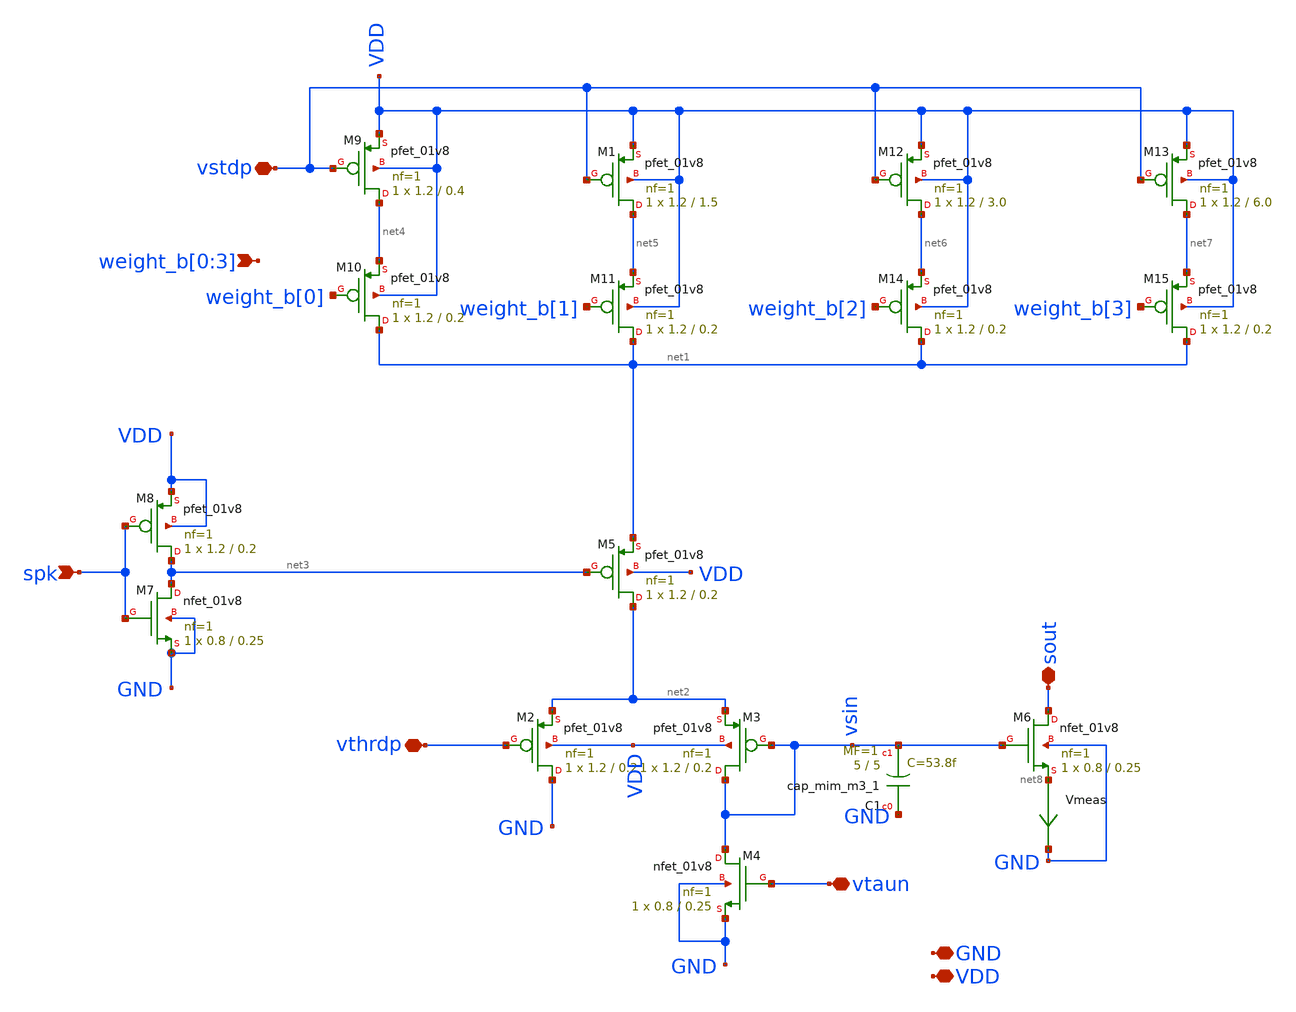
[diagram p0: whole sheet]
** sch_path: design/xschem/dpi_syn_inh_4bit_fc.sch
**.subckt dpi_syn_inh_4bit_fc spk vstdp vthrdp vtaun sout GND VDD
*+ weight_b[0],weight_b[1],weight_b[2],weight_b[3]
*.ipin spk
*.iopin vstdp
*.iopin vthrdp
*.iopin vtaun
*.iopin sout
*.iopin GND
*.iopin VDD
*.ipin weight_b[0],weight_b[1],weight_b[2],weight_b[3]
XM5 net2 net3 net1 VDD sky130_fd_pr__pfet_01v8 L=0.2 W=1.2 nf=1 ad='int((nf+1)/2) * W/nf * 0.29' as='int((nf+2)/2) * W/nf * 0.29'
+ pd='2*int((nf+1)/2) * (W/nf + 0.29)' ps='2*int((nf+2)/2) * (W/nf + 0.29)' nrd='0.29 / W' nrs='0.29 / W'
+ sa=0 sb=0 sd=0 mult=1 m=1
XM2 GND vthrdp net2 VDD sky130_fd_pr__pfet_01v8 L=0.2 W=1.2 nf=1 ad='int((nf+1)/2) * W/nf * 0.29' as='int((nf+2)/2) * W/nf * 0.29'
+ pd='2*int((nf+1)/2) * (W/nf + 0.29)' ps='2*int((nf+2)/2) * (W/nf + 0.29)' nrd='0.29 / W' nrs='0.29 / W'
+ sa=0 sb=0 sd=0 mult=1 m=1
XM3 vsin vsin net2 VDD sky130_fd_pr__pfet_01v8 L=0.2 W=1.2 nf=1 ad='int((nf+1)/2) * W/nf * 0.29' as='int((nf+2)/2) * W/nf * 0.29'
+ pd='2*int((nf+1)/2) * (W/nf + 0.29)' ps='2*int((nf+2)/2) * (W/nf + 0.29)' nrd='0.29 / W' nrs='0.29 / W'
+ sa=0 sb=0 sd=0 mult=1 m=1
XM4 vsin vtaun GND GND sky130_fd_pr__nfet_01v8 L=0.25 W=0.8 nf=1 ad='int((nf+1)/2) * W/nf * 0.29' as='int((nf+2)/2) * W/nf * 0.29'
+ pd='2*int((nf+1)/2) * (W/nf + 0.29)' ps='2*int((nf+2)/2) * (W/nf + 0.29)' nrd='0.29 / W' nrs='0.29 / W'
+ sa=0 sb=0 sd=0 mult=1 m=1
XM6 sout vsin net8 GND sky130_fd_pr__nfet_01v8 L=0.25 W=0.8 nf=1 ad='int((nf+1)/2) * W/nf * 0.29' as='int((nf+2)/2) * W/nf * 0.29'
+ pd='2*int((nf+1)/2) * (W/nf + 0.29)' ps='2*int((nf+2)/2) * (W/nf + 0.29)' nrd='0.29 / W' nrs='0.29 / W'
+ sa=0 sb=0 sd=0 mult=1 m=1
XM7 net3 spk GND GND sky130_fd_pr__nfet_01v8 L=0.25 W=0.8 nf=1 ad='int((nf+1)/2) * W/nf * 0.29' as='int((nf+2)/2) * W/nf * 0.29'
+ pd='2*int((nf+1)/2) * (W/nf + 0.29)' ps='2*int((nf+2)/2) * (W/nf + 0.29)' nrd='0.29 / W' nrs='0.29 / W'
+ sa=0 sb=0 sd=0 mult=1 m=1
XM8 net3 spk VDD VDD sky130_fd_pr__pfet_01v8 L=0.2 W=1.2 nf=1 ad='int((nf+1)/2) * W/nf * 0.29' as='int((nf+2)/2) * W/nf * 0.29'
+ pd='2*int((nf+1)/2) * (W/nf + 0.29)' ps='2*int((nf+2)/2) * (W/nf + 0.29)' nrd='0.29 / W' nrs='0.29 / W'
+ sa=0 sb=0 sd=0 mult=1 m=1
XC1 GND vsin sky130_fd_pr__cap_mim_m3_1 W=5 L=5 MF=1 m=1
XM9 net4 vstdp VDD VDD sky130_fd_pr__pfet_01v8 L=0.4 W=1.2 nf=1 ad='int((nf+1)/2) * W/nf * 0.29' as='int((nf+2)/2) * W/nf * 0.29'
+ pd='2*int((nf+1)/2) * (W/nf + 0.29)' ps='2*int((nf+2)/2) * (W/nf + 0.29)' nrd='0.29 / W' nrs='0.29 / W'
+ sa=0 sb=0 sd=0 mult=1 m=1
XM10 net1 weight_b[0] net4 VDD sky130_fd_pr__pfet_01v8 L=0.2 W=1.2 nf=1 ad='int((nf+1)/2) * W/nf * 0.29'
+ as='int((nf+2)/2) * W/nf * 0.29' pd='2*int((nf+1)/2) * (W/nf + 0.29)' ps='2*int((nf+2)/2) * (W/nf + 0.29)'
+ nrd='0.29 / W' nrs='0.29 / W' sa=0 sb=0 sd=0 mult=1 m=1
XM11 net1 weight_b[1] net5 VDD sky130_fd_pr__pfet_01v8 L=0.2 W=1.2 nf=1 ad='int((nf+1)/2) * W/nf * 0.29'
+ as='int((nf+2)/2) * W/nf * 0.29' pd='2*int((nf+1)/2) * (W/nf + 0.29)' ps='2*int((nf+2)/2) * (W/nf + 0.29)'
+ nrd='0.29 / W' nrs='0.29 / W' sa=0 sb=0 sd=0 mult=1 m=1
XM1 net5 vstdp VDD VDD sky130_fd_pr__pfet_01v8 L=1.5 W=1.2 nf=1 ad='int((nf+1)/2) * W/nf * 0.29' as='int((nf+2)/2) * W/nf * 0.29'
+ pd='2*int((nf+1)/2) * (W/nf + 0.29)' ps='2*int((nf+2)/2) * (W/nf + 0.29)' nrd='0.29 / W' nrs='0.29 / W'
+ sa=0 sb=0 sd=0 mult=1 m=1
XM12 net6 vstdp VDD VDD sky130_fd_pr__pfet_01v8 L=3.0 W=1.2 nf=1 ad='int((nf+1)/2) * W/nf * 0.29' as='int((nf+2)/2) * W/nf * 0.29'
+ pd='2*int((nf+1)/2) * (W/nf + 0.29)' ps='2*int((nf+2)/2) * (W/nf + 0.29)' nrd='0.29 / W' nrs='0.29 / W'
+ sa=0 sb=0 sd=0 mult=1 m=1
XM13 net7 vstdp VDD VDD sky130_fd_pr__pfet_01v8 L=6.0 W=1.2 nf=1 ad='int((nf+1)/2) * W/nf * 0.29' as='int((nf+2)/2) * W/nf * 0.29'
+ pd='2*int((nf+1)/2) * (W/nf + 0.29)' ps='2*int((nf+2)/2) * (W/nf + 0.29)' nrd='0.29 / W' nrs='0.29 / W'
+ sa=0 sb=0 sd=0 mult=1 m=1
XM14 net1 weight_b[2] net6 VDD sky130_fd_pr__pfet_01v8 L=0.2 W=1.2 nf=1 ad='int((nf+1)/2) * W/nf * 0.29'
+ as='int((nf+2)/2) * W/nf * 0.29' pd='2*int((nf+1)/2) * (W/nf + 0.29)' ps='2*int((nf+2)/2) * (W/nf + 0.29)'
+ nrd='0.29 / W' nrs='0.29 / W' sa=0 sb=0 sd=0 mult=1 m=1
XM15 net1 weight_b[3] net7 VDD sky130_fd_pr__pfet_01v8 L=0.2 W=1.2 nf=1 ad='int((nf+1)/2) * W/nf * 0.29'
+ as='int((nf+2)/2) * W/nf * 0.29' pd='2*int((nf+1)/2) * (W/nf + 0.29)' ps='2*int((nf+2)/2) * (W/nf + 0.29)'
+ nrd='0.29 / W' nrs='0.29 / W' sa=0 sb=0 sd=0 mult=1 m=1
Vmeas net8 GND 0
.save i(vmeas)
**.ends
.end
